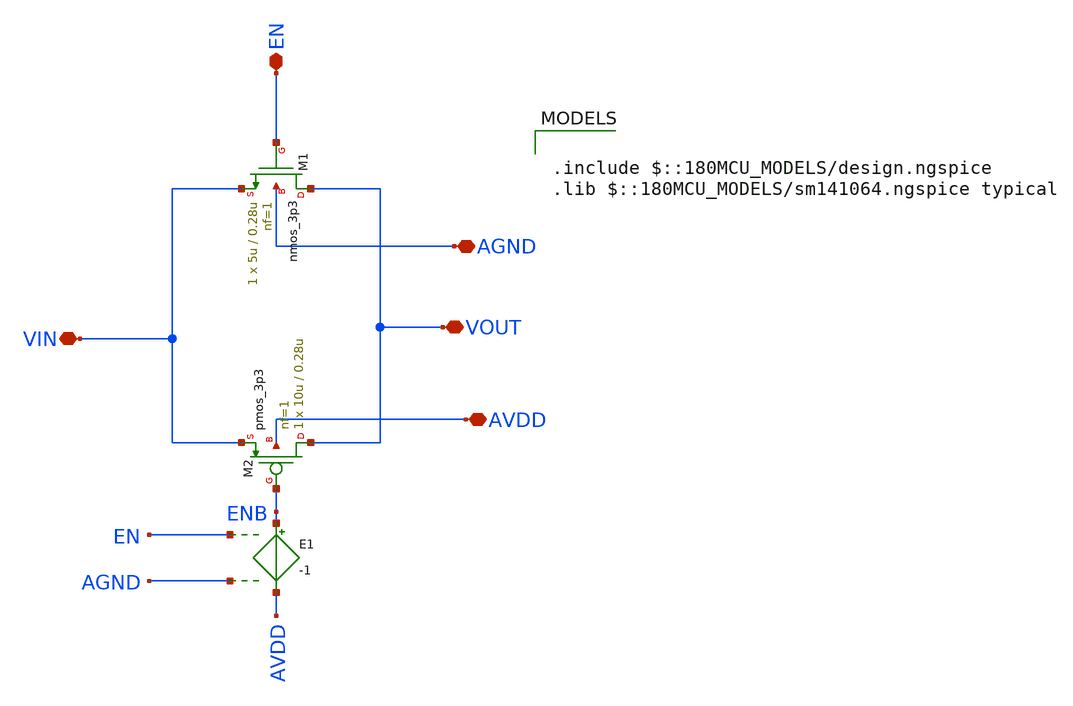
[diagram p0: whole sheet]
** sch_path: XSCHEM Files/tg.sch
**.subckt tg AGND AVDD VOUT VIN EN
*.iopin AGND
*.iopin AVDD
*.iopin VOUT
*.iopin VIN
*.iopin EN
XM1 VOUT EN VIN AGND nmos_3p3 L=0.28u W=5u nf=1 ad='int((nf+1)/2) * W/nf * 0.18u' as='int((nf+2)/2) * W/nf * 0.18u'
+ pd='2*int((nf+1)/2) * (W/nf + 0.18u)' ps='2*int((nf+2)/2) * (W/nf + 0.18u)' nrd='0.18u / W' nrs='0.18u / W'
+ sa=0 sb=0 sd=0 m=1
XM2 VOUT ENB VIN AVDD pmos_3p3 L=0.28u W=10u nf=1 ad='int((nf+1)/2) * W/nf * 0.18u' as='int((nf+2)/2) * W/nf * 0.18u'
+ pd='2*int((nf+1)/2) * (W/nf + 0.18u)' ps='2*int((nf+2)/2) * (W/nf + 0.18u)' nrd='0.18u / W' nrs='0.18u / W'
+ sa=0 sb=0 sd=0 m=1
E1 ENB AVDD EN AGND -1
**** begin user architecture code

.include $::180MCU_MODELS/design.ngspice
.lib $::180MCU_MODELS/sm141064.ngspice typical

**** end user architecture code
**.ends
.end
